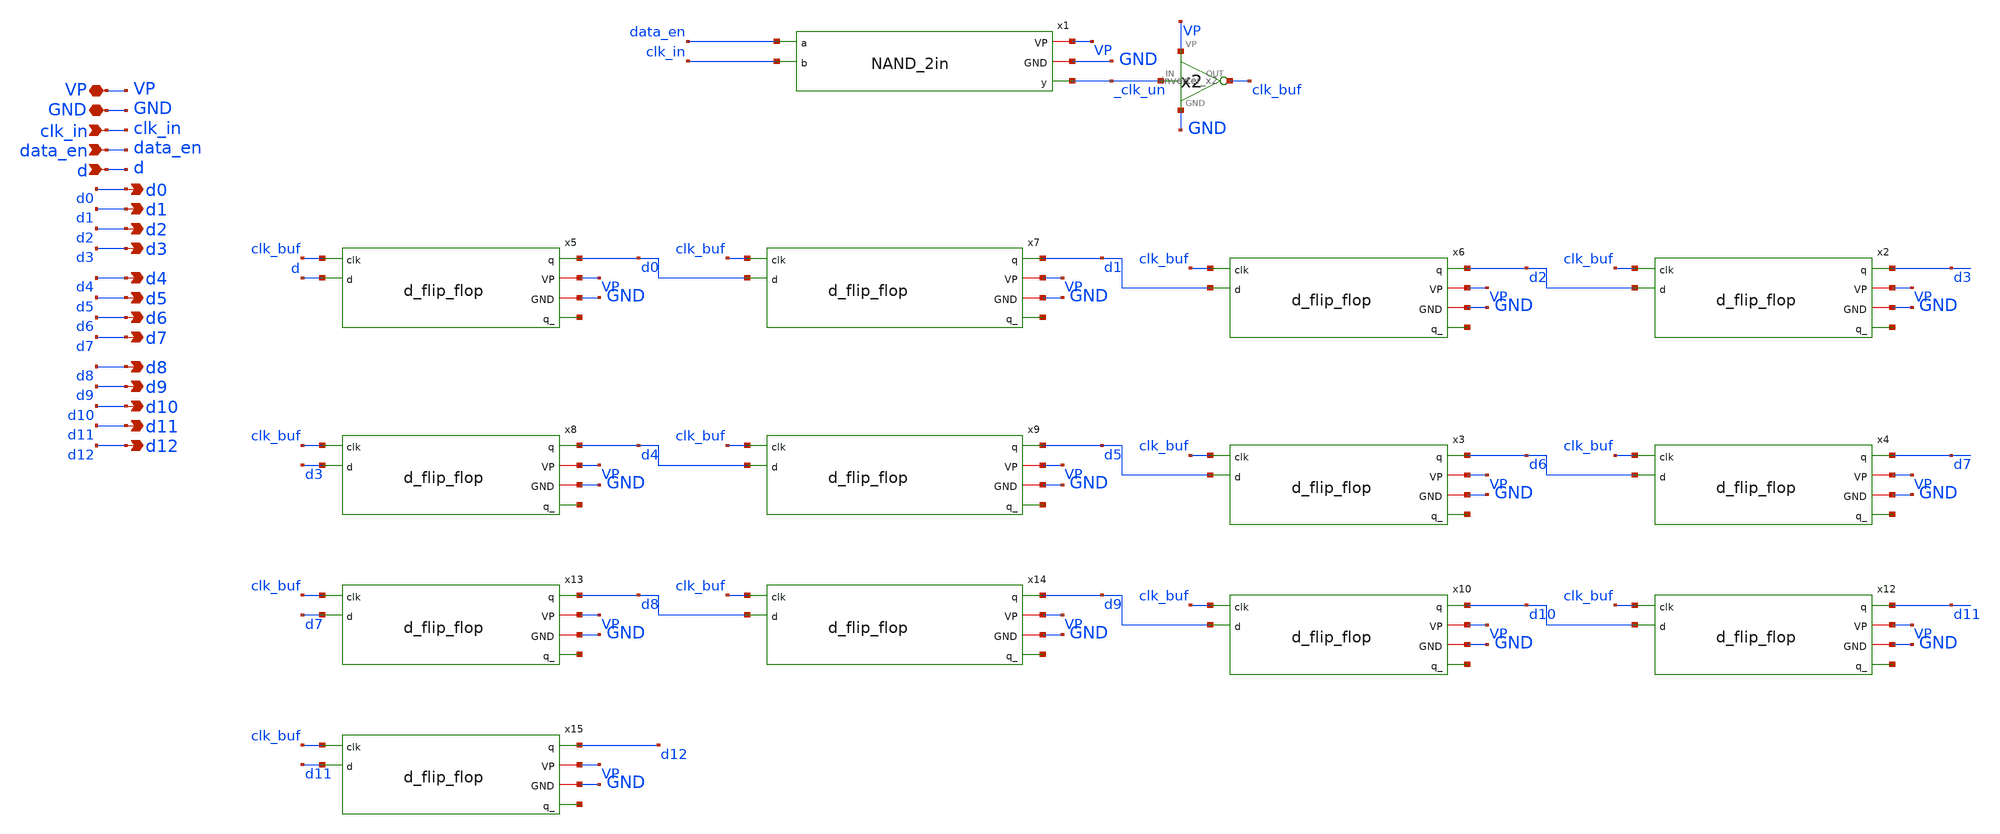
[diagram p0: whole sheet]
** sch_path: schematics/divider/schematics/input_register.sch
**.subckt input_register VP clk_in GND data_en d d0 d2 d3 d4 d5 d6 d7 d1 d8 d9 d10 d11 d12
*.iopin VP
*.ipin clk_in
*.iopin GND
*.ipin data_en
*.ipin d
*.opin d0
*.opin d2
*.opin d3
*.opin d4
*.opin d5
*.opin d6
*.opin d7
*.opin d1
*.opin d8
*.opin d9
*.opin d10
*.opin d11
*.opin d12
x1 VP GND data_en _clk_un clk_in NAND_2in
x6 d2 VP GND net1 clk_buf d1 d_flip_flop
x2 d3 VP GND net2 clk_buf d2 d_flip_flop
x3 d6 VP GND net3 clk_buf d5 d_flip_flop
x4 d7 VP GND net4 clk_buf d6 d_flip_flop
x5 d0 VP GND net5 clk_buf d d_flip_flop
x7 d1 VP GND net6 clk_buf d0 d_flip_flop
x8 d4 VP GND net7 clk_buf d3 d_flip_flop
x9 d5 VP GND net8 clk_buf d4 d_flip_flop
x10 d10 VP GND net9 clk_buf d9 d_flip_flop
x12 d11 VP GND net10 clk_buf d10 d_flip_flop
x13 d8 VP GND net11 clk_buf d7 d_flip_flop
x14 d9 VP GND net12 clk_buf d8 d_flip_flop
x15 d12 VP GND net13 clk_buf d11 d_flip_flop
x11 _clk_un clk_buf VP GND inverter_x2
**.ends
.end
